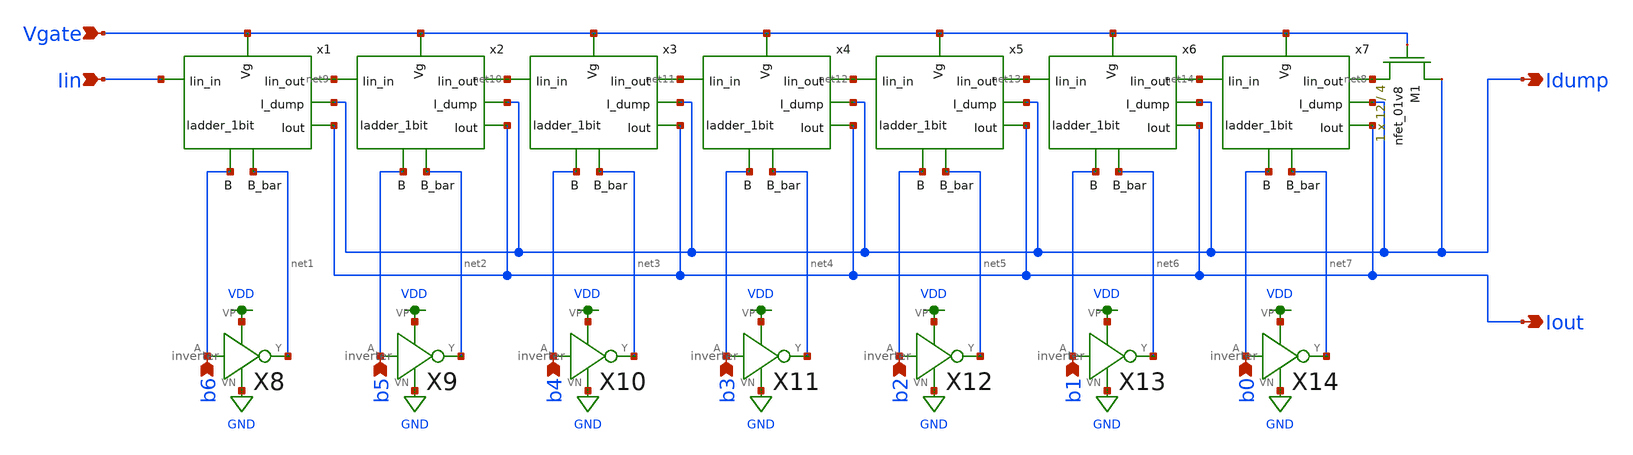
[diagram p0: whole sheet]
** sch_path: modules/ladder_7bit.sch
**.subckt ladder_7bit Idump Vgate Iin b6 b5 b4 b3 b2 b1 b0 Iout
*.opin Idump
*.ipin Vgate
*.ipin Iin
*.ipin b6
*.ipin b5
*.ipin b4
*.ipin b3
*.ipin b2
*.ipin b1
*.ipin b0
*.opin Iout
XM1 Idump Vgate net8 GND sky130_fd_pr__nfet_01v8 L=4 W=12 nf=1 ad='int((nf+1)/2) * W/nf * 0.29' as='int((nf+2)/2) * W/nf * 0.29'
+ pd='2*int((nf+1)/2) * (W/nf + 0.29)' ps='2*int((nf+2)/2) * (W/nf + 0.29)' nrd='0.29 / W' nrs='0.29 / W'
+ sa=0 sb=0 sd=0 mult=1 m=1
x1 Iin net9 Vgate Idump Iout net1 b6 ladder_1bit
X8 b6 net1 VDD GND inverter
x2 net9 net10 Vgate Idump Iout net2 b5 ladder_1bit
x3 net10 net11 Vgate Idump Iout net3 b4 ladder_1bit
x4 net11 net12 Vgate Idump Iout net4 b3 ladder_1bit
x5 net12 net13 Vgate Idump Iout net5 b2 ladder_1bit
x6 net13 net14 Vgate Idump Iout net6 b1 ladder_1bit
x7 net14 net8 Vgate Idump Iout net7 b0 ladder_1bit
X9 b5 net2 VDD GND inverter
X10 b4 net3 VDD GND inverter
X11 b3 net4 VDD GND inverter
X12 b2 net5 VDD GND inverter
X13 b1 net6 VDD GND inverter
X14 b0 net7 VDD GND inverter
**.ends

* expanding   symbol:  ../modules/ladder_1bit.sym # of pins=7
** sym_path: modules/ladder_1bit.sym
** sch_path: modules/ladder_1bit.sch
.subckt ladder_1bit Iin_in Iin_out Vg I_dump Iout B_bar B
*.ipin Iin_in
*.ipin Vg
*.ipin B
*.ipin B_bar
*.opin Iin_out
*.opin I_dump
*.opin Iout
XM5 net1 Vg Iin_in GND sky130_fd_pr__nfet_01v8 L=0.15 W=1 nf=1 ad='int((nf+1)/2) * W/nf * 0.29' as='int((nf+2)/2) * W/nf * 0.29'
+ pd='2*int((nf+1)/2) * (W/nf + 0.29)' ps='2*int((nf+2)/2) * (W/nf + 0.29)' nrd='0.29 / W' nrs='0.29 / W'
+ sa=0 sb=0 sd=0 mult=1 m=1
XM6 Iout B net1 GND sky130_fd_pr__nfet_01v8 L=0.15 W=1 nf=1 ad='int((nf+1)/2) * W/nf * 0.29' as='int((nf+2)/2) * W/nf * 0.29'
+ pd='2*int((nf+1)/2) * (W/nf + 0.29)' ps='2*int((nf+2)/2) * (W/nf + 0.29)' nrd='0.29 / W' nrs='0.29 / W'
+ sa=0 sb=0 sd=0 mult=1 m=1
XM7 net1 B_bar I_dump GND sky130_fd_pr__nfet_01v8 L=0.15 W=1 nf=1 ad='int((nf+1)/2) * W/nf * 0.29' as='int((nf+2)/2) * W/nf * 0.29'
+ pd='2*int((nf+1)/2) * (W/nf + 0.29)' ps='2*int((nf+2)/2) * (W/nf + 0.29)' nrd='0.29 / W' nrs='0.29 / W'
+ sa=0 sb=0 sd=0 mult=1 m=1
XM8 Iin_in Vg Iin_out GND sky130_fd_pr__nfet_01v8 L=0.15 W=1 nf=1 ad='int((nf+1)/2) * W/nf * 0.29' as='int((nf+2)/2) * W/nf * 0.29'
+ pd='2*int((nf+1)/2) * (W/nf + 0.29)' ps='2*int((nf+2)/2) * (W/nf + 0.29)' nrd='0.29 / W' nrs='0.29 / W'
+ sa=0 sb=0 sd=0 mult=1 m=1
.ends


* expanding   symbol:  ../modules/inverter.sym # of pins=4
** sym_path: modules/inverter.sym
** sch_path: modules/inverter.sch
.subckt inverter A Y VP VN
*.ipin A
*.iopin VP
*.iopin VN
*.opin Y
XM3 Y A VP VP sky130_fd_pr__pfet_01v8 L=0.15 W=1 nf=1 ad='int((nf+1)/2) * W/nf * 0.29' as='int((nf+2)/2) * W/nf * 0.29'
+ pd='2*int((nf+1)/2) * (W/nf + 0.29)' ps='2*int((nf+2)/2) * (W/nf + 0.29)' nrd='0.29 / W' nrs='0.29 / W'
+ sa=0 sb=0 sd=0 mult=1 m=1
XM4 Y A VN VN sky130_fd_pr__nfet_01v8 L=0.15 W=1 nf=1 ad='int((nf+1)/2) * W/nf * 0.29' as='int((nf+2)/2) * W/nf * 0.29'
+ pd='2*int((nf+1)/2) * (W/nf + 0.29)' ps='2*int((nf+2)/2) * (W/nf + 0.29)' nrd='0.29 / W' nrs='0.29 / W'
+ sa=0 sb=0 sd=0 mult=1 m=1
.ends

.GLOBAL VDD
.GLOBAL GND
.end
